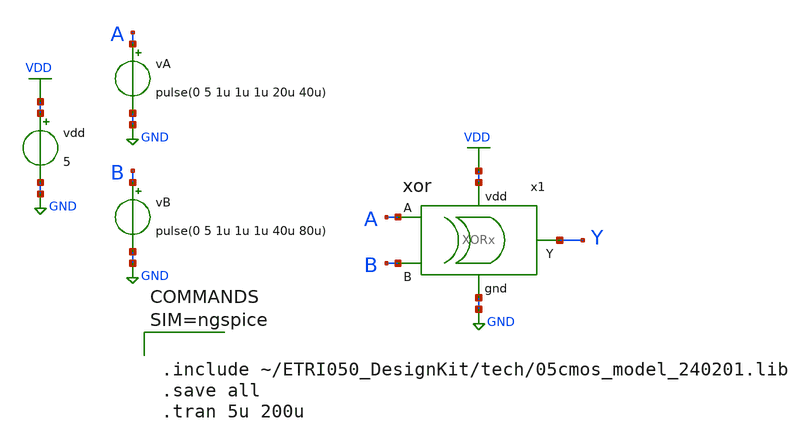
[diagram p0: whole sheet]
** sch_path: lab7/sch/made/tb_xor.sch
**.subckt tb_xor
x1 VDD GND A B Y XORx
vA A GND pulse(0 5 1u 1u 1u 20u 40u)
vB B GND pulse(0 5 1u 1u 1u 40u 80u)
vdd VDD GND 5
**** begin user architecture code



.include ~/ETRI050_DesignKit/tech/05cmos_model_240201.lib
.save all
.tran 5u 200u



**** end user architecture code
**.ends

* expanding   symbol:  /home/dayesong/ETRI050_DesignKit/lab7/sch/XORx.sym # of pins=5
** sym_path: lab7/sch/made/XORx.sym
** sch_path: lab7/sch/made/XORx.sch
.subckt XORx vdd gnd A B Y
*.ipin A
*.ipin B
*.opin Y
*.iopin vdd
*.iopin gnd
x4 vdd A net1 B gnd NORx
x2 vdd net1 net4 gnd INVx
x3 vdd net3 net2 net4 gnd NANDx
x5 vdd net2 Y gnd INVx
x1 vdd A net3 B gnd NANDx
.ends


* expanding   symbol:  /home/dayesong/ETRI050_DesignKit/lab7/sch/NORx.sym # of pins=5
** sym_path: lab7/sch/made/NORx.sym
** sch_path: lab7/sch/made/NORx.sch
.subckt NORx vdd A Y B gnd
*.ipin A
*.ipin B
*.opin Y
*.iopin vdd
*.iopin gnd
M1 net1 A vdd vdd pfet w=12u l=0.6u m=1
M2 Y B net1 vdd pfet w=12u l=0.6u m=1
M3 Y B gnd gnd nfet w=3u l=0.6u m=1
M4 Y A gnd gnd nfet w=3u l=0.6u m=1
.ends


* expanding   symbol:  /home/dayesong/ETRI050_DesignKit/lab7/sch/INVx.sym # of pins=4
** sym_path: lab7/sch/made/INVx.sym
** sch_path: lab7/sch/made/INVx.sch
.subckt INVx vdd A Y gnd
*.ipin A
*.opin Y
*.iopin vdd
*.iopin gnd
M1 Y A vdd vdd pfet w=6u l=0.6u m=1
M2 Y A gnd gnd nfet w=3u l=0.6u m=1
.ends


* expanding   symbol:  /home/dayesong/ETRI050_DesignKit/lab7/sch/NANDx.sym # of pins=5
** sym_path: lab7/sch/made/NANDx.sym
** sch_path: lab7/sch/made/NANDx.sch
.subckt NANDx vdd A Y B gnd
*.ipin A
*.ipin B
*.opin Y
*.iopin vdd
*.iopin gnd
M3 Y B net1 gnd nfet w=6u l=0.6u m=1
M4 Y B vdd vdd pfet w=6u l=0.6u m=1
M2 Y A vdd vdd pfet w=6u l=0.6u m=1
M1 net1 A gnd gnd nfet w=6u l=0.6u m=1
.ends

.GLOBAL VDD
.GLOBAL GND
.end
